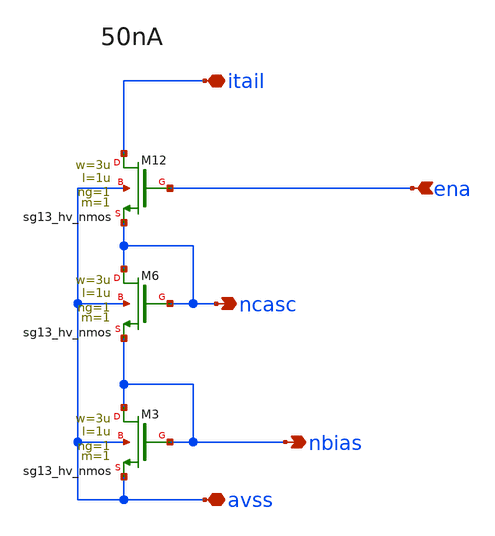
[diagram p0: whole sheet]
** sch_path: xschem/bias_nset.sch
**.subckt bias_nset avss ena itail nbias ncasc
*.iopin avss
*.ipin ena
*.iopin itail
*.opin nbias
*.opin ncasc
XM3 nbias nbias avss avss sg13_hv_nmos w=3u l=1u ng=1 m=1 mm_ok=1
XM6 ncasc ncasc nbias avss sg13_hv_nmos w=3u l=1u ng=1 m=1 mm_ok=1
XM12 itail ena ncasc avss sg13_hv_nmos w=3u l=1u ng=1 m=1 mm_ok=1
**.ends
.end
